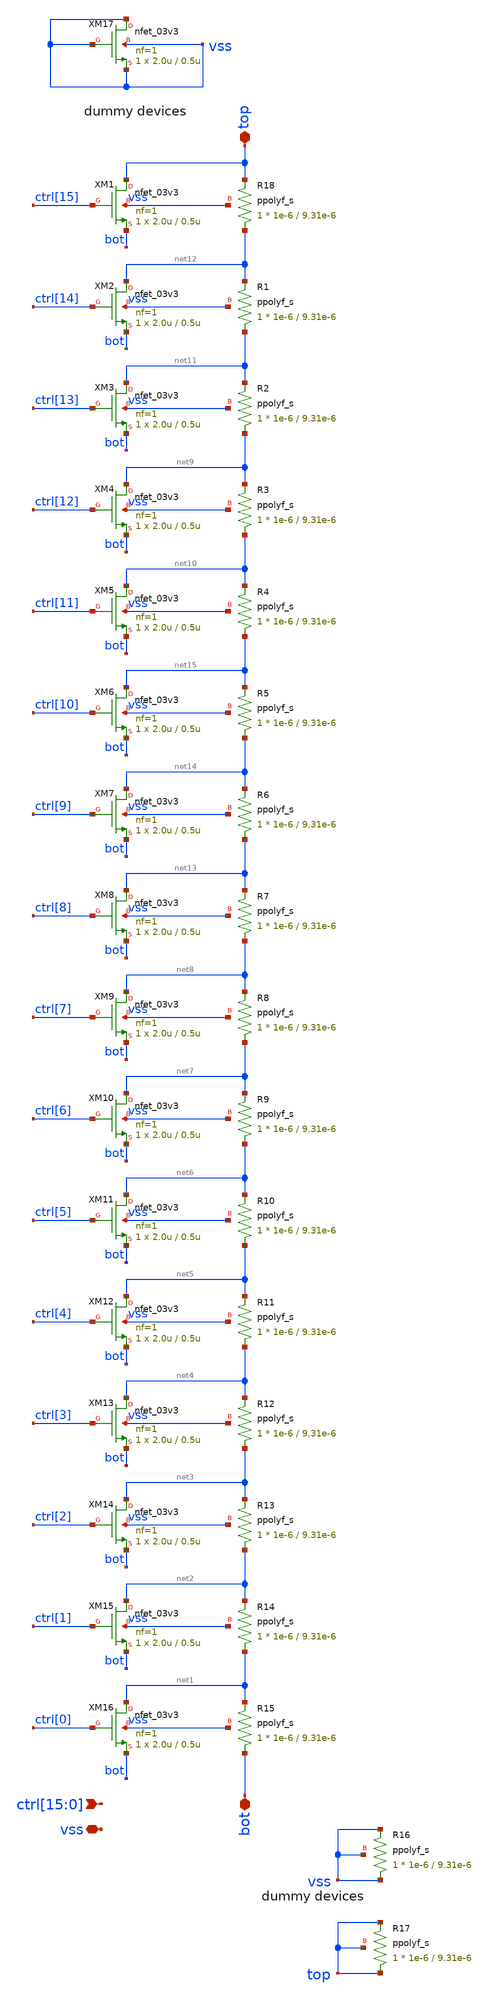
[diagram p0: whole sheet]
** sch_path: xschem/bg_trim.sch
**.subckt bg_trim vss
*+ ctrl[15],ctrl[14],ctrl[13],ctrl[12],ctrl[11],ctrl[10],ctrl[9],ctrl[8],ctrl[7],ctrl[6],ctrl[5],ctrl[4],ctrl[3],ctrl[2],ctrl[1],ctrl[0] bot top
*.iopin vss
*.ipin
*+ ctrl[15],ctrl[14],ctrl[13],ctrl[12],ctrl[11],ctrl[10],ctrl[9],ctrl[8],ctrl[7],ctrl[6],ctrl[5],ctrl[4],ctrl[3],ctrl[2],ctrl[1],ctrl[0]
*.iopin bot
*.iopin top
XM17 vss vss vss vss nfet_03v3 L=0.5u W=2.0u nf=1 ad='int((nf+1)/2) * W/nf * 0.18u' as='int((nf+2)/2) * W/nf * 0.18u'
+ pd='2*int((nf+1)/2) * (W/nf + 0.18u)' ps='2*int((nf+2)/2) * (W/nf + 0.18u)' nrd='0.18u / W' nrs='0.18u / W'
+ sa=0 sb=0 sd=0 m=1 par=1
XM1 top ctrl[15] bot vss nfet_03v3 L=0.5u W=2.0u nf=1 ad='int((nf+1)/2) * W/nf * 0.18u' as='int((nf+2)/2) * W/nf * 0.18u'
+ pd='2*int((nf+1)/2) * (W/nf + 0.18u)' ps='2*int((nf+2)/2) * (W/nf + 0.18u)' nrd='0.18u / W' nrs='0.18u / W'
+ sa=0 sb=0 sd=0 m=1 par=1
XM2 net12 ctrl[14] bot vss nfet_03v3 L=0.5u W=2.0u nf=1 ad='int((nf+1)/2) * W/nf * 0.18u' as='int((nf+2)/2) * W/nf * 0.18u'
+ pd='2*int((nf+1)/2) * (W/nf + 0.18u)' ps='2*int((nf+2)/2) * (W/nf + 0.18u)' nrd='0.18u / W' nrs='0.18u / W'
+ sa=0 sb=0 sd=0 m=1 par=1
XM3 net11 ctrl[13] bot vss nfet_03v3 L=0.5u W=2.0u nf=1 ad='int((nf+1)/2) * W/nf * 0.18u' as='int((nf+2)/2) * W/nf * 0.18u'
+ pd='2*int((nf+1)/2) * (W/nf + 0.18u)' ps='2*int((nf+2)/2) * (W/nf + 0.18u)' nrd='0.18u / W' nrs='0.18u / W'
+ sa=0 sb=0 sd=0 m=1 par=1
XM4 net9 ctrl[12] bot vss nfet_03v3 L=0.5u W=2.0u nf=1 ad='int((nf+1)/2) * W/nf * 0.18u' as='int((nf+2)/2) * W/nf * 0.18u'
+ pd='2*int((nf+1)/2) * (W/nf + 0.18u)' ps='2*int((nf+2)/2) * (W/nf + 0.18u)' nrd='0.18u / W' nrs='0.18u / W'
+ sa=0 sb=0 sd=0 m=1 par=1
XM5 net10 ctrl[11] bot vss nfet_03v3 L=0.5u W=2.0u nf=1 ad='int((nf+1)/2) * W/nf * 0.18u' as='int((nf+2)/2) * W/nf * 0.18u'
+ pd='2*int((nf+1)/2) * (W/nf + 0.18u)' ps='2*int((nf+2)/2) * (W/nf + 0.18u)' nrd='0.18u / W' nrs='0.18u / W'
+ sa=0 sb=0 sd=0 m=1 par=1
XM6 net15 ctrl[10] bot vss nfet_03v3 L=0.5u W=2.0u nf=1 ad='int((nf+1)/2) * W/nf * 0.18u' as='int((nf+2)/2) * W/nf * 0.18u'
+ pd='2*int((nf+1)/2) * (W/nf + 0.18u)' ps='2*int((nf+2)/2) * (W/nf + 0.18u)' nrd='0.18u / W' nrs='0.18u / W'
+ sa=0 sb=0 sd=0 m=1 par=1
XM7 net14 ctrl[9] bot vss nfet_03v3 L=0.5u W=2.0u nf=1 ad='int((nf+1)/2) * W/nf * 0.18u' as='int((nf+2)/2) * W/nf * 0.18u'
+ pd='2*int((nf+1)/2) * (W/nf + 0.18u)' ps='2*int((nf+2)/2) * (W/nf + 0.18u)' nrd='0.18u / W' nrs='0.18u / W'
+ sa=0 sb=0 sd=0 m=1 par=1
XM8 net13 ctrl[8] bot vss nfet_03v3 L=0.5u W=2.0u nf=1 ad='int((nf+1)/2) * W/nf * 0.18u' as='int((nf+2)/2) * W/nf * 0.18u'
+ pd='2*int((nf+1)/2) * (W/nf + 0.18u)' ps='2*int((nf+2)/2) * (W/nf + 0.18u)' nrd='0.18u / W' nrs='0.18u / W'
+ sa=0 sb=0 sd=0 m=1 par=1
XM9 net8 ctrl[7] bot vss nfet_03v3 L=0.5u W=2.0u nf=1 ad='int((nf+1)/2) * W/nf * 0.18u' as='int((nf+2)/2) * W/nf * 0.18u'
+ pd='2*int((nf+1)/2) * (W/nf + 0.18u)' ps='2*int((nf+2)/2) * (W/nf + 0.18u)' nrd='0.18u / W' nrs='0.18u / W'
+ sa=0 sb=0 sd=0 m=1 par=1
XM10 net7 ctrl[6] bot vss nfet_03v3 L=0.5u W=2.0u nf=1 ad='int((nf+1)/2) * W/nf * 0.18u' as='int((nf+2)/2) * W/nf * 0.18u'
+ pd='2*int((nf+1)/2) * (W/nf + 0.18u)' ps='2*int((nf+2)/2) * (W/nf + 0.18u)' nrd='0.18u / W' nrs='0.18u / W'
+ sa=0 sb=0 sd=0 m=1 par=1
XM11 net6 ctrl[5] bot vss nfet_03v3 L=0.5u W=2.0u nf=1 ad='int((nf+1)/2) * W/nf * 0.18u' as='int((nf+2)/2) * W/nf * 0.18u'
+ pd='2*int((nf+1)/2) * (W/nf + 0.18u)' ps='2*int((nf+2)/2) * (W/nf + 0.18u)' nrd='0.18u / W' nrs='0.18u / W'
+ sa=0 sb=0 sd=0 m=1 par=1
XM12 net5 ctrl[4] bot vss nfet_03v3 L=0.5u W=2.0u nf=1 ad='int((nf+1)/2) * W/nf * 0.18u' as='int((nf+2)/2) * W/nf * 0.18u'
+ pd='2*int((nf+1)/2) * (W/nf + 0.18u)' ps='2*int((nf+2)/2) * (W/nf + 0.18u)' nrd='0.18u / W' nrs='0.18u / W'
+ sa=0 sb=0 sd=0 m=1 par=1
XM13 net4 ctrl[3] bot vss nfet_03v3 L=0.5u W=2.0u nf=1 ad='int((nf+1)/2) * W/nf * 0.18u' as='int((nf+2)/2) * W/nf * 0.18u'
+ pd='2*int((nf+1)/2) * (W/nf + 0.18u)' ps='2*int((nf+2)/2) * (W/nf + 0.18u)' nrd='0.18u / W' nrs='0.18u / W'
+ sa=0 sb=0 sd=0 m=1 par=1
XM14 net3 ctrl[2] bot vss nfet_03v3 L=0.5u W=2.0u nf=1 ad='int((nf+1)/2) * W/nf * 0.18u' as='int((nf+2)/2) * W/nf * 0.18u'
+ pd='2*int((nf+1)/2) * (W/nf + 0.18u)' ps='2*int((nf+2)/2) * (W/nf + 0.18u)' nrd='0.18u / W' nrs='0.18u / W'
+ sa=0 sb=0 sd=0 m=1 par=1
XM15 net2 ctrl[1] bot vss nfet_03v3 L=0.5u W=2.0u nf=1 ad='int((nf+1)/2) * W/nf * 0.18u' as='int((nf+2)/2) * W/nf * 0.18u'
+ pd='2*int((nf+1)/2) * (W/nf + 0.18u)' ps='2*int((nf+2)/2) * (W/nf + 0.18u)' nrd='0.18u / W' nrs='0.18u / W'
+ sa=0 sb=0 sd=0 m=1 par=1
XM16 net1 ctrl[0] bot vss nfet_03v3 L=0.5u W=2.0u nf=1 ad='int((nf+1)/2) * W/nf * 0.18u' as='int((nf+2)/2) * W/nf * 0.18u'
+ pd='2*int((nf+1)/2) * (W/nf + 0.18u)' ps='2*int((nf+2)/2) * (W/nf + 0.18u)' nrd='0.18u / W' nrs='0.18u / W'
+ sa=0 sb=0 sd=0 m=1 par=1
XR18 net12 top vss ppolyf_s r_width=1e-6 r_length=9.31e-6 m=1
XR1 net11 net12 vss ppolyf_s r_width=1e-6 r_length=9.31e-6 m=1
XR2 net9 net11 vss ppolyf_s r_width=1e-6 r_length=9.31e-6 m=1
XR3 net10 net9 vss ppolyf_s r_width=1e-6 r_length=9.31e-6 m=1
XR4 net15 net10 vss ppolyf_s r_width=1e-6 r_length=9.31e-6 m=1
XR5 net14 net15 vss ppolyf_s r_width=1e-6 r_length=9.31e-6 m=1
XR6 net13 net14 vss ppolyf_s r_width=1e-6 r_length=9.31e-6 m=1
XR7 net8 net13 vss ppolyf_s r_width=1e-6 r_length=9.31e-6 m=1
XR8 net7 net8 vss ppolyf_s r_width=1e-6 r_length=9.31e-6 m=1
XR9 net6 net7 vss ppolyf_s r_width=1e-6 r_length=9.31e-6 m=1
XR10 net5 net6 vss ppolyf_s r_width=1e-6 r_length=9.31e-6 m=1
XR11 net4 net5 vss ppolyf_s r_width=1e-6 r_length=9.31e-6 m=1
XR12 net3 net4 vss ppolyf_s r_width=1e-6 r_length=9.31e-6 m=1
XR13 net2 net3 vss ppolyf_s r_width=1e-6 r_length=9.31e-6 m=1
XR14 net1 net2 vss ppolyf_s r_width=1e-6 r_length=9.31e-6 m=1
XR15 bot net1 vss ppolyf_s r_width=1e-6 r_length=9.31e-6 m=1
XR16 vss vss vss ppolyf_s r_width=1e-6 r_length=9.31e-6 m=1
XR17 top top top ppolyf_s r_width=1e-6 r_length=9.31e-6 m=1
**.ends
.end
